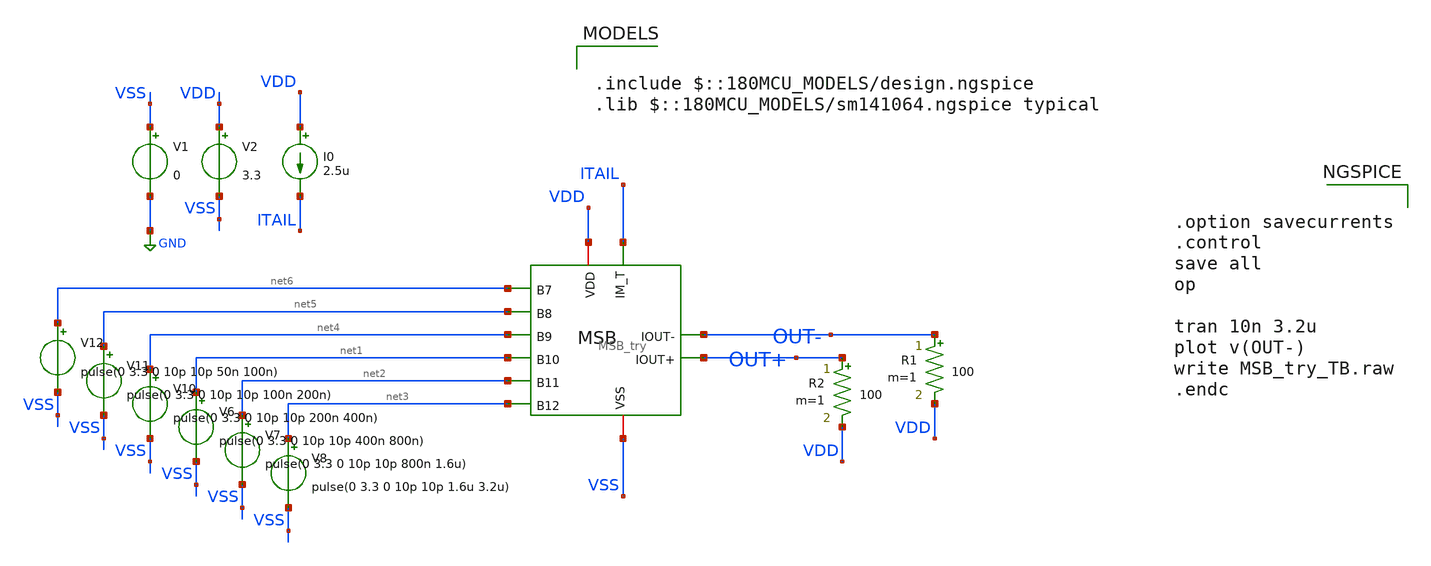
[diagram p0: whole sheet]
** sch_path: DAC_PAKISTAN_01/Pakistan1_Xschem/MSB_try_TB.sch
**.subckt MSB_try_TB
V1 VSS GND 0
V2 VDD VSS 3.3
V6 net1 VSS pulse(0 3.3 0 10p 10p 400n 800n)
V7 net2 VSS pulse(0 3.3 0 10p 10p 800n 1.6u)
V8 net3 VSS pulse(0 3.3 0 10p 10p 1.6u 3.2u)
V10 net4 VSS pulse(0 3.3 0 10p 10p 200n 400n)
V11 net5 VSS pulse(0 3.3 0 10p 10p 100n 200n)
V12 net6 VSS pulse(0 3.3 0 10p 10p 50n 100n)
R1 OUT- VDD 100 m=1
R2 OUT+ VDD 100 m=1
I0 VDD ITAIL 2.5u
x1 VSS VDD net2 net6 net5 net3 net4 ITAIL net1 OUT- OUT+ MSB_try
**** begin user architecture code

.include $::180MCU_MODELS/design.ngspice
.lib $::180MCU_MODELS/sm141064.ngspice typical



.option savecurrents
.control
save all
op

tran 10n 3.2u
plot v(OUT-)
write MSB_try_TB.raw
.endc


**** end user architecture code
**.ends
.GLOBAL GND
.end
